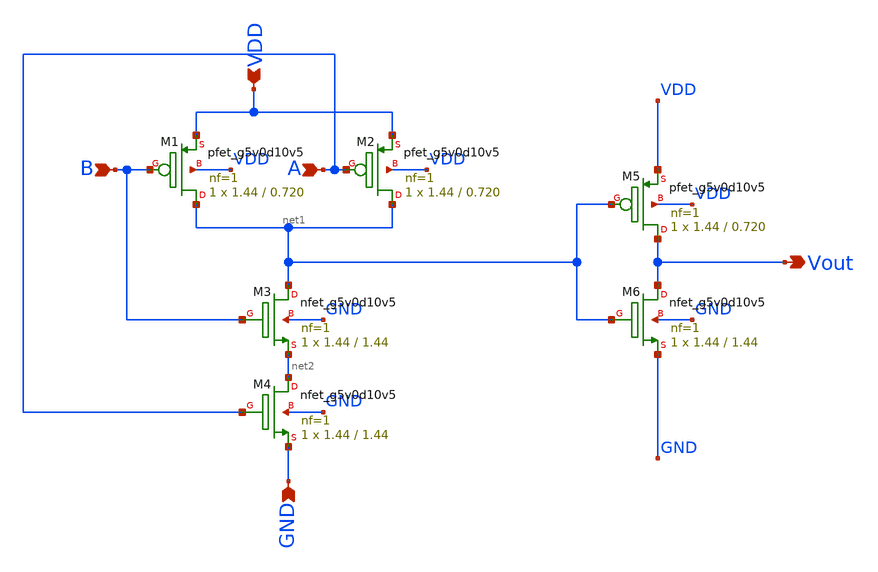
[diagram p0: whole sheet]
** sch_path: xschem/And_Gate.sch
**.subckt And_Gate Vout A B VDD GND
*.opin Vout
*.ipin A
*.ipin B
*.ipin VDD
*.ipin GND
XM1 net1 B VDD VDD sky130_fd_pr__pfet_g5v0d10v5 L=0.720 W=1.44 nf=1 ad='int((1 + 1)/2) * 1.44 / 1 * 0.29'
+ as='int((1 + 2)/2) * 1.44 / 1 * 0.29' pd='2*int((1 + 1)/2) * (1.44 / 1 + 0.29)' ps='2*int((1 + 2)/2) * (1.44 / 1 + 0.29)'
+ nrd='0.29 / 1.44 ' nrs='0.29 / 1.44 ' sa=0 sb=0 sd=0 mult=1 m=1
XM2 net1 A VDD VDD sky130_fd_pr__pfet_g5v0d10v5 L=0.720 W=1.44 nf=1 ad='int((1 + 1)/2) * 1.44 / 1 * 0.29'
+ as='int((1 + 2)/2) * 1.44 / 1 * 0.29' pd='2*int((1 + 1)/2) * (1.44 / 1 + 0.29)' ps='2*int((1 + 2)/2) * (1.44 / 1 + 0.29)'
+ nrd='0.29 / 1.44 ' nrs='0.29 / 1.44 ' sa=0 sb=0 sd=0 mult=1 m=1
XM3 net1 B net2 GND sky130_fd_pr__nfet_g5v0d10v5 L=1.44 W=1.44 nf=1 ad='int((1 + 1)/2) * 1.44 / 1 * 0.29'
+ as='int((1 + 2)/2) * 1.44 / 1 * 0.29' pd='2*int((1 + 1)/2) * (1.44 / 1 + 0.29)' ps='2*int((1 + 2)/2) * (1.44 / 1 + 0.29)'
+ nrd='0.29 / 1.44 ' nrs='0.29 / 1.44 ' sa=0 sb=0 sd=0 mult=1 m=1
XM4 net2 A GND GND sky130_fd_pr__nfet_g5v0d10v5 L=1.44 W=1.44 nf=1 ad='int((1 + 1)/2) * 1.44 / 1 * 0.29'
+ as='int((1 + 2)/2) * 1.44 / 1 * 0.29' pd='2*int((1 + 1)/2) * (1.44 / 1 + 0.29)' ps='2*int((1 + 2)/2) * (1.44 / 1 + 0.29)'
+ nrd='0.29 / 1.44 ' nrs='0.29 / 1.44 ' sa=0 sb=0 sd=0 mult=1 m=1
XM5 Vout net1 VDD VDD sky130_fd_pr__pfet_g5v0d10v5 L=0.720 W=1.44 nf=1 ad='int((1 + 1)/2) * 1.44 / 1 * 0.29'
+ as='int((1 + 2)/2) * 1.44 / 1 * 0.29' pd='2*int((1 + 1)/2) * (1.44 / 1 + 0.29)' ps='2*int((1 + 2)/2) * (1.44 / 1 + 0.29)'
+ nrd='0.29 / 1.44 ' nrs='0.29 / 1.44 ' sa=0 sb=0 sd=0 mult=1 m=1
XM6 Vout net1 GND GND sky130_fd_pr__nfet_g5v0d10v5 L=1.44 W=1.44 nf=1 ad='int((1 + 1)/2) * 1.44 / 1 * 0.29'
+ as='int((1 + 2)/2) * 1.44 / 1 * 0.29' pd='2*int((1 + 1)/2) * (1.44 / 1 + 0.29)' ps='2*int((1 + 2)/2) * (1.44 / 1 + 0.29)'
+ nrd='0.29 / 1.44 ' nrs='0.29 / 1.44 ' sa=0 sb=0 sd=0 mult=1 m=1
**.ends
.end
